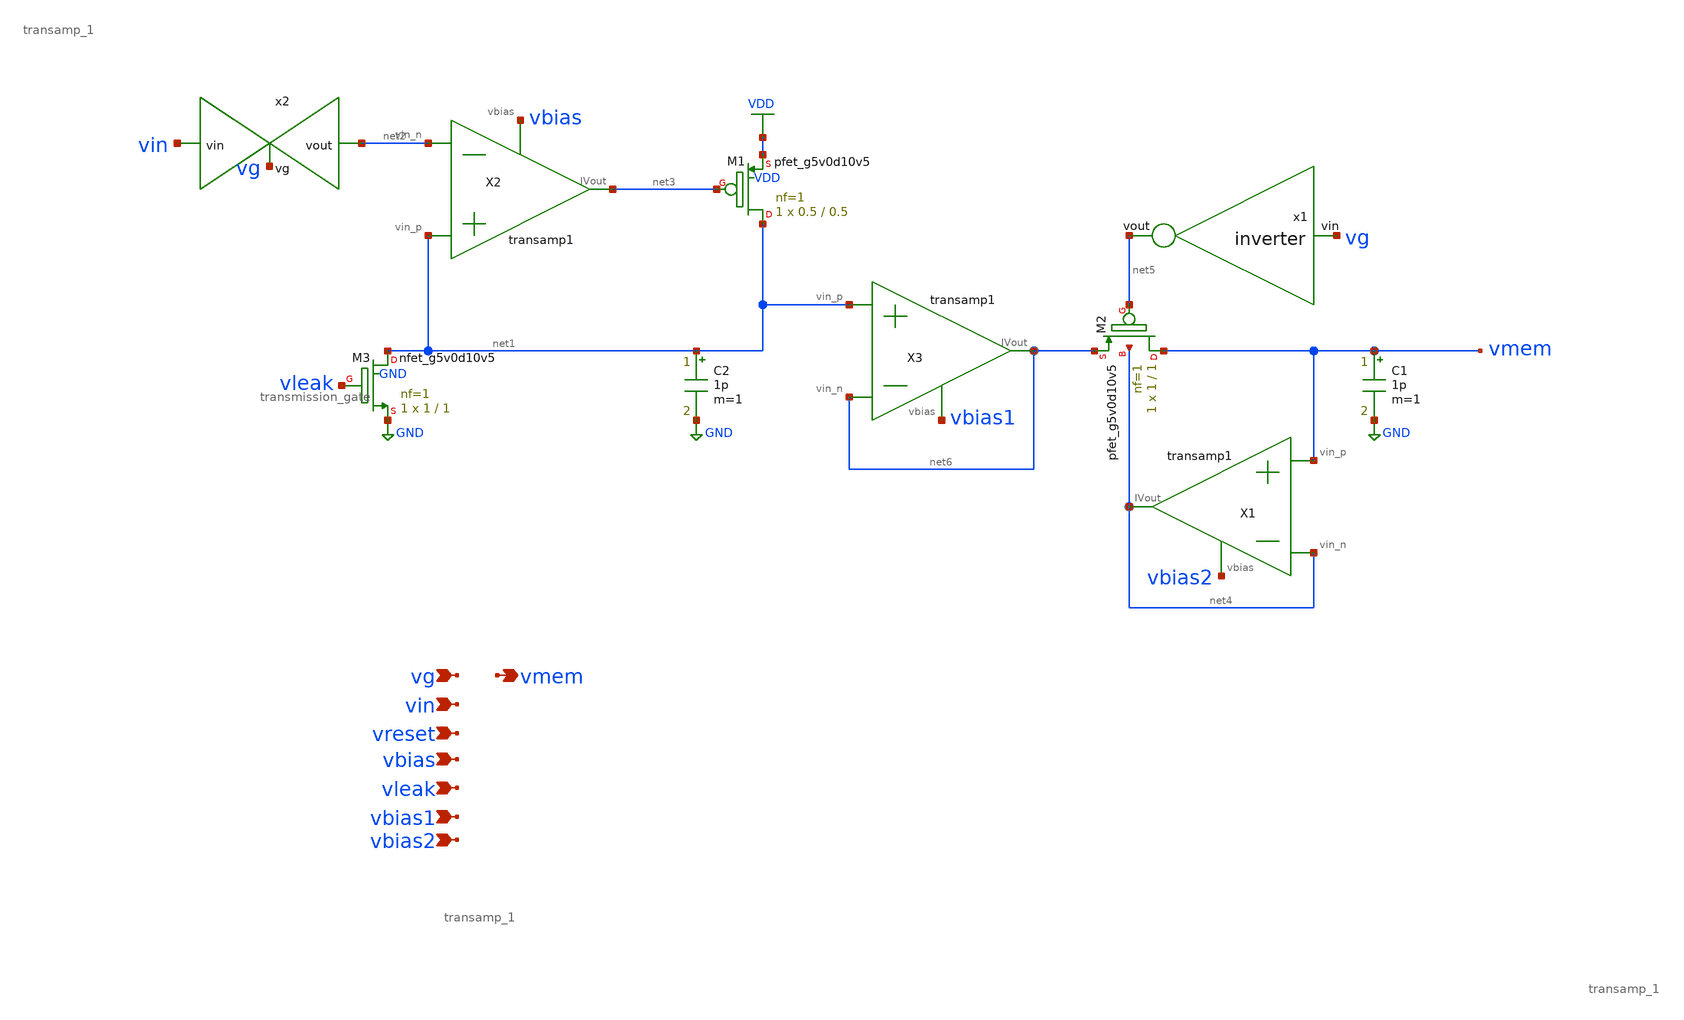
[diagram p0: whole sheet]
** sch_path: schematics/cap_mem1.sch
**.subckt cap_mem1 vg vin vreset vbias vleak vmem vbias1 vbias2
*.ipin vg
*.ipin vin
*.ipin vreset
*.ipin vbias
*.ipin vleak
*.opin vmem
*.ipin vbias1
*.ipin vbias2
XM1 net1 net3 VDD VDD sky130_fd_pr__pfet_g5v0d10v5 L=0.5 W=0.5 nf=1 ad='int((nf+1)/2) * W/nf * 0.29'
+ as='int((nf+2)/2) * W/nf * 0.29' pd='2*int((nf+1)/2) * (W/nf + 0.29)' ps='2*int((nf+2)/2) * (W/nf + 0.29)'
+ nrd='0.29 / W' nrs='0.29 / W' sa=0 sb=0 sd=0 mult=1 m=1
C2 net1 GND 1p m=1
X2 net1 net2 net3 vbias transamp_1
x2 vin net2 vg transmission_gate
XM2 vmem net5 net6 net4 sky130_fd_pr__pfet_g5v0d10v5 L=1 W=1 nf=1 ad='int((nf+1)/2) * W/nf * 0.29' as='int((nf+2)/2) * W/nf * 0.29'
+ pd='2*int((nf+1)/2) * (W/nf + 0.29)' ps='2*int((nf+2)/2) * (W/nf + 0.29)' nrd='0.29 / W' nrs='0.29 / W'
+ sa=0 sb=0 sd=0 mult=1 m=1
X1 vmem net4 net4 vbias2 transamp_1
C1 vmem GND 1p m=1
x1 net5 vg inverter
X3 net1 net6 net6 vbias1 transamp_1
XM3 net1 vleak GND GND sky130_fd_pr__nfet_g5v0d10v5 L=1 W=1 nf=1 ad='int((nf+1)/2) * W/nf * 0.29' as='int((nf+2)/2) * W/nf * 0.29'
+ pd='2*int((nf+1)/2) * (W/nf + 0.29)' ps='2*int((nf+2)/2) * (W/nf + 0.29)' nrd='0.29 / W' nrs='0.29 / W'
+ sa=0 sb=0 sd=0 mult=1 m=1
**.ends

* expanding   symbol:  /media/sf_share/final_project/transamp_1.sym # of pins=4
** sym_path: schematics/transamp_1.sym
** sch_path: schematics/transamp_1.sch
.subckt transamp_1 vin_p vin_n IVout vbias
*.opin IVout
*.ipin vin_p
*.ipin vin_n
*.ipin vbias
XM1 net1 vbias GND GND sky130_fd_pr__nfet_g5v0d10v5 L=1 W=1 nf=1 ad='int((nf+1)/2) * W/nf * 0.29' as='int((nf+2)/2) * W/nf * 0.29'
+ pd='2*int((nf+1)/2) * (W/nf + 0.29)' ps='2*int((nf+2)/2) * (W/nf + 0.29)' nrd='0.29 / W' nrs='0.29 / W'
+ sa=0 sb=0 sd=0 mult=1 m=1
XM3 net2 vin_p net1 GND sky130_fd_pr__nfet_g5v0d10v5 L=1 W=1 nf=1 ad='int((nf+1)/2) * W/nf * 0.29' as='int((nf+2)/2) * W/nf * 0.29'
+ pd='2*int((nf+1)/2) * (W/nf + 0.29)' ps='2*int((nf+2)/2) * (W/nf + 0.29)' nrd='0.29 / W' nrs='0.29 / W'
+ sa=0 sb=0 sd=0 mult=1 m=1
XM4 IVout net2 VDD VDD sky130_fd_pr__pfet_g5v0d10v5 L=1 W=1 nf=1 ad='int((nf+1)/2) * W/nf * 0.29' as='int((nf+2)/2) * W/nf * 0.29'
+ pd='2*int((nf+1)/2) * (W/nf + 0.29)' ps='2*int((nf+2)/2) * (W/nf + 0.29)' nrd='0.29 / W' nrs='0.29 / W'
+ sa=0 sb=0 sd=0 mult=1 m=1
XM2 IVout vin_n net1 GND sky130_fd_pr__nfet_g5v0d10v5 L=1 W=1 nf=1 ad='int((nf+1)/2) * W/nf * 0.29' as='int((nf+2)/2) * W/nf * 0.29'
+ pd='2*int((nf+1)/2) * (W/nf + 0.29)' ps='2*int((nf+2)/2) * (W/nf + 0.29)' nrd='0.29 / W' nrs='0.29 / W'
+ sa=0 sb=0 sd=0 mult=1 m=1
XM5 net2 net2 VDD VDD sky130_fd_pr__pfet_g5v0d10v5 L=1 W=1 nf=1 ad='int((nf+1)/2) * W/nf * 0.29' as='int((nf+2)/2) * W/nf * 0.29'
+ pd='2*int((nf+1)/2) * (W/nf + 0.29)' ps='2*int((nf+2)/2) * (W/nf + 0.29)' nrd='0.29 / W' nrs='0.29 / W'
+ sa=0 sb=0 sd=0 mult=1 m=1
.ends


* expanding   symbol:  /media/sf_share/final_project/transmission_gate.sym # of pins=3
** sym_path: schematics/transmission_gate.sym
** sch_path: schematics/transmission_gate.sch
.subckt transmission_gate vin vout vg
*.ipin vin
*.ipin vg
*.opin vout
x1 vg_bar vg inverter
XM5 vin vg vout GND sky130_fd_pr__nfet_g5v0d10v5 L=0.5 W=0.5 nf=1 ad='int((nf+1)/2) * W/nf * 0.29' as='int((nf+2)/2) * W/nf * 0.29'
+ pd='2*int((nf+1)/2) * (W/nf + 0.29)' ps='2*int((nf+2)/2) * (W/nf + 0.29)' nrd='0.29 / W' nrs='0.29 / W'
+ sa=0 sb=0 sd=0 mult=1 m=1
XM7 vout vg_bar vin VDD sky130_fd_pr__pfet_g5v0d10v5 L=0.5 W=0.5 nf=1 ad='int((nf+1)/2) * W/nf * 0.29'
+ as='int((nf+2)/2) * W/nf * 0.29' pd='2*int((nf+1)/2) * (W/nf + 0.29)' ps='2*int((nf+2)/2) * (W/nf + 0.29)'
+ nrd='0.29 / W' nrs='0.29 / W' sa=0 sb=0 sd=0 mult=1 m=1
XM6 vout vg_bar GND GND sky130_fd_pr__nfet_g5v0d10v5 L=0.5 W=0.5 nf=1 ad='int((nf+1)/2) * W/nf * 0.29'
+ as='int((nf+2)/2) * W/nf * 0.29' pd='2*int((nf+1)/2) * (W/nf + 0.29)' ps='2*int((nf+2)/2) * (W/nf + 0.29)'
+ nrd='0.29 / W' nrs='0.29 / W' sa=0 sb=0 sd=0 mult=1 m=1
.ends


* expanding   symbol:  /media/sf_share/final_project/inverter.sym # of pins=2
** sym_path: schematics/inverter.sym
** sch_path: schematics/inverter.sch
.subckt inverter vout vin
*.ipin vin
*.opin vout
XM3 vout vin VDD VDD sky130_fd_pr__pfet_g5v0d10v5 L=0.5 W=0.5 nf=1 ad='int((nf+1)/2) * W/nf * 0.29' as='int((nf+2)/2) * W/nf * 0.29'
+ pd='2*int((nf+1)/2) * (W/nf + 0.29)' ps='2*int((nf+2)/2) * (W/nf + 0.29)' nrd='0.29 / W' nrs='0.29 / W'
+ sa=0 sb=0 sd=0 mult=1 m=1
XM5 vout vin GND GND sky130_fd_pr__nfet_g5v0d10v5 L=0.5 W=0.5 nf=1 ad='int((nf+1)/2) * W/nf * 0.29' as='int((nf+2)/2) * W/nf * 0.29'
+ pd='2*int((nf+1)/2) * (W/nf + 0.29)' ps='2*int((nf+2)/2) * (W/nf + 0.29)' nrd='0.29 / W' nrs='0.29 / W'
+ sa=0 sb=0 sd=0 mult=1 m=1
.ends

.GLOBAL VDD
.GLOBAL GND
.end
